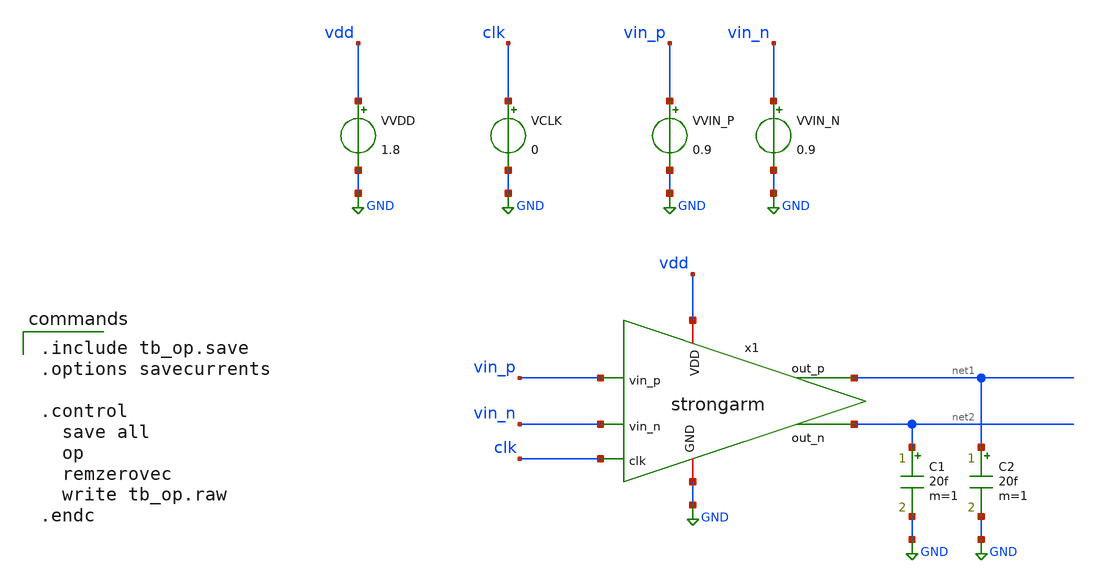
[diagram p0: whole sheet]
** sch_path: 01_xschem_ngspice/soluzioni/lab03/xschem/tb_op.sch
**.subckt tb_op
VVDD vdd GND 1.8
VCLK clk GND 0
VVIN_P vin_p GND 0.9
VVIN_N vin_n GND 0.9
C1 net2 GND 20f m=1
C2 net1 GND 20f m=1
x1 vdd net1 net2 vin_p vin_n clk GND strongarm
**** begin user architecture code

** opencircuitdesign pdks install
.lib $::SKYWATER_MODELS/sky130.lib.spice tt


.include tb_op.save
.options savecurrents

.control
  save all
  op
  remzerovec
  write tb_op.raw
.endc

**** end user architecture code
**.ends
.GLOBAL GND
.end
